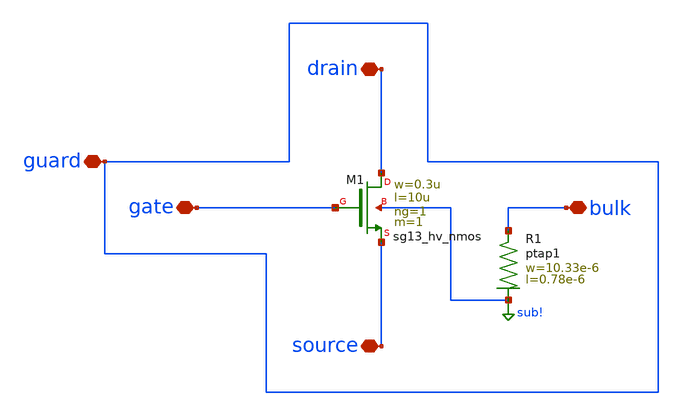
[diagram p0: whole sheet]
** sch_path: trident_test_structures/design_data/xschem/transistor_characterization/hv_nmos_w0u3_l10u0_guarded/hv_nmos_w0u3_l10u0_guarded.sch
**.subckt hv_nmos_w0u3_l10u0_guarded gate drain source bulk guard
*.iopin gate
*.iopin drain
*.iopin source
*.iopin bulk
*.iopin guard
XM1 drain gate source sub! sg13_hv_nmos w=0.3u l=10u ng=1 m=1 mm_ok=1
XR1 bulk sub! ptap1 R=32.37 w=10.33e-6 l=0.78e-6
**.ends
.GLOBAL sub!
.end
